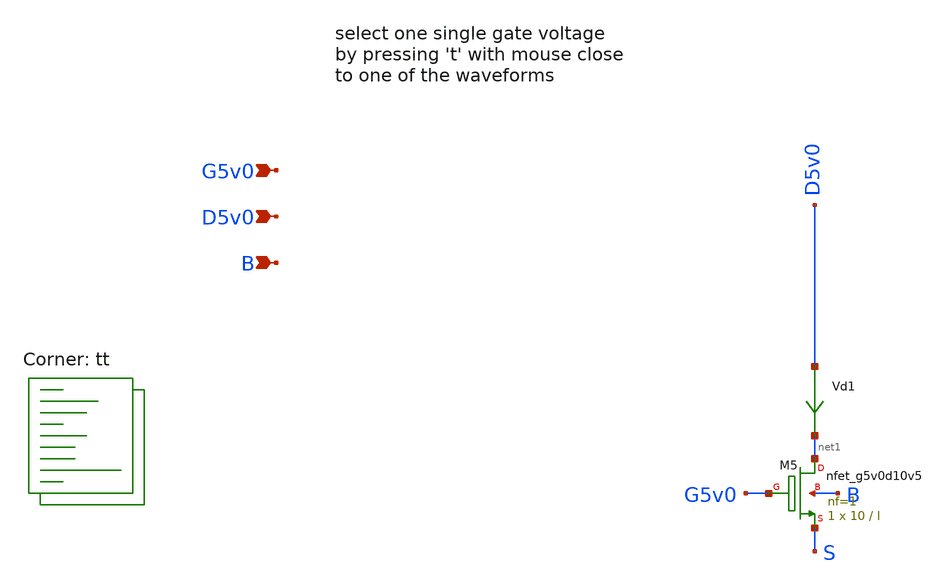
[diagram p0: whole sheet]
** sch_path: userLib/test_nmos2.sch
**.subckt test_nmos2 G5v0 D5v0 B
*.ipin G5v0
*.ipin D5v0
*.ipin B
Vd1 D5v0 net1 0
.save i(vd1)
XM5 net1 G5v0 S B sky130_fd_pr__nfet_g5v0d10v5 L=l W=10 nf=1 ad='int((1 + 1)/2) * 10 / 1 * 0.29' as='int((1 + 2)/2) * 10 / 1 * 0.29'
+ pd='2*int((1 + 1)/2) * (10 / 1 + 0.29)' ps='2*int((1 + 2)/2) * (10 / 1 + 0.29)' nrd='0.29 / 10 ' nrs='0.29 / 10 '
+ sa=0 sb=0 sd=0 mult=1 m=1
**** begin user architecture code

* this option enables mos model bin
* selection based on W/NF instead of W
.option wnflag=1
.option savecurrents
.param l = 0.5
vg G5v0 0 1.3
vs s 0 0
vd D5v0 0 3.3
vb b 0 0
.control
save all
let loop_start = 0.5
let loop_end = 10
let loop_delta = 0.5
let loop_act = loop_start


save @m.xm5.msky130_fd_pr__nfet_g5v0d10v5[gm]
save @m.xm5.msky130_fd_pr__nfet_g5v0d10v5[gds]
save @m.xm5.msky130_fd_pr__nfet_g5v0d10v5[vth]
save @m.xm5.msky130_fd_pr__nfet_g5v0d10v5[cgg]

print all.@m.xm5.msky130_fd_pr__nfet_g5v0d10v5[gm]
print all.@m.xm5.msky130_fd_pr__nfet_g5v0d10v5[gds]
print all.@m.xm5.msky130_fd_pr__nfet_g5v0d10v5[vth]
print all.@m.xm5.msky130_fd_pr__nfet_g5v0d10v5[cgg]

while loop_act le loop_end
  alter l loop_act
  dc vd 0 3.3 0.01 vg 0 3.3 0.9
  write test_nmos2.raw
  *dc vd 0 3.3 0.01 vg 0 3.3 0.9
  let loop_act = loop_act + loop_delta
 end
plot all.vd1#branch vs D5v0

plot all.@m.xm5.msky130_fd_pr__nfet_g5v0d10v5[gds] vs D5v0
plot all.@m.xm5.msky130_fd_pr__nfet_g5v0d10v5[vth] vs D5v0
plot all.@m.xm5.msky130_fd_pr__nfet_g5v0d10v5[cgg] vs D5v0
plot all.@m.xm5.msky130_fd_pr__nfet_g5v0d10v5[gm] vs i(vd1)
plot all.@m.xm5.msky130_fd_pr__nfet_g5v0d10v5[gds] vs G5v0
plot all.@m.xm5.msky130_fd_pr__nfet_g5v0d10v5[vth] vs G5v0
plot all.@m.xm5.msky130_fd_pr__nfet_g5v0d10v5[cgg] vs G5v0
set appendwrite
set filetype=binary
write test_nmos2.raw
set wr_singlescale
set wr_vecnames
wrdata nmosParams.txt all.@m.xm5.msky130_fd_pr__nfet_g5v0d10v5[gm]
+ all.@m.xm5.msky130_fd_pr__nfet_g5v0d10v5[gds] all.@m.xm5.msky130_fd_pr__nfet_g5v0d10v5[vth] all.@m.xm5.msky130_fd_pr__nfet_g5v0d10v5[cgg]
+ all.i(Vd1)

.endc


.lib $::SKYWATER_MODELS/sky130.lib.spice tt
**** end user architecture code
**.ends
.end
